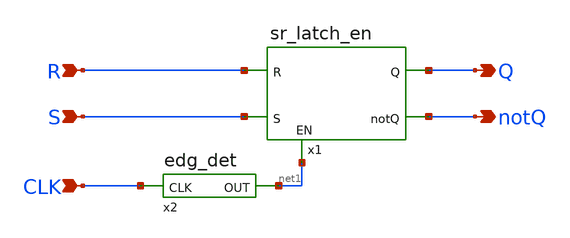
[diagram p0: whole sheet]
** sch_path: Circuiti/latches_sch_sym/sr_flip_flop_short.sch
**.subckt sr_flip_flop_short R S Q notQ CLK
*.ipin R
*.ipin S
*.opin Q
*.opin notQ
*.ipin CLK
x1 R Q net1 notQ S sr_latch_en
x2 net1 CLK edg_det
**.ends
.end
